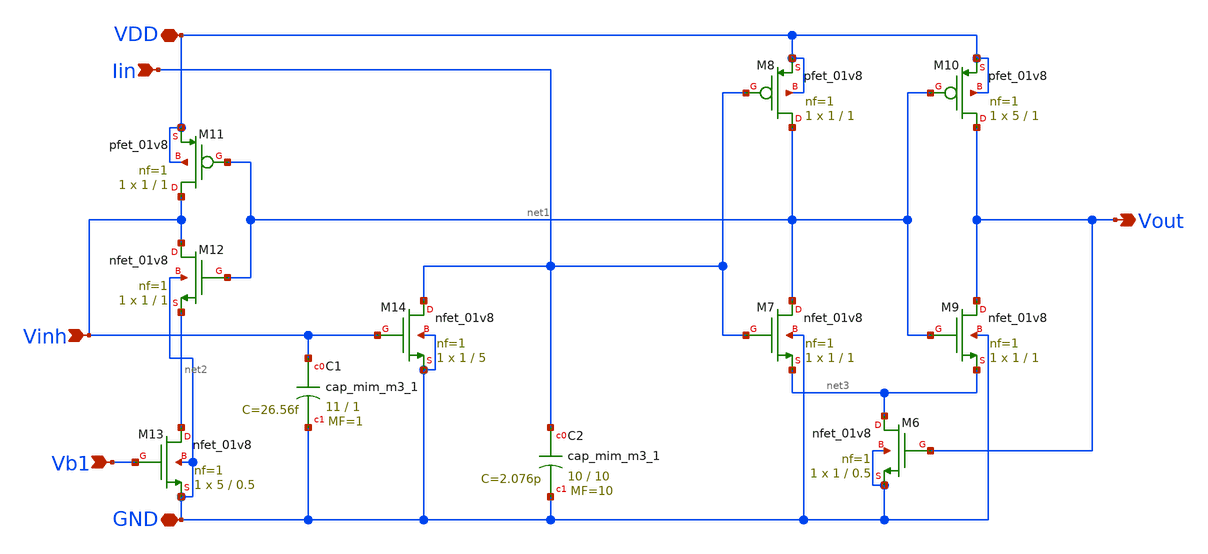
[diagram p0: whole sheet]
** sch_path: LIF_neuron/Postsynaptic_LIF_neuron.sch
**.subckt Postsynaptic_LIF_neuron GND Vb1 VDD Vout Iin Vinh
*.iopin GND
*.ipin Vb1
*.iopin VDD
*.opin Vout
*.ipin Iin
*.ipin Vinh
XM13 net2 Vb1 GND GND sky130_fd_pr__nfet_01v8 L=0.5 W=5 nf=1 ad='int((nf+1)/2) * W/nf * 0.29' as='int((nf+2)/2) * W/nf * 0.29'
+ pd='2*int((nf+1)/2) * (W/nf + 0.29)' ps='2*int((nf+2)/2) * (W/nf + 0.29)' nrd='0.29 / W' nrs='0.29 / W'
+ sa=0 sb=0 sd=0 mult=1 m=1
XM12 Vinh net1 net2 GND sky130_fd_pr__nfet_01v8 L=1 W=1 nf=1 ad='int((nf+1)/2) * W/nf * 0.29' as='int((nf+2)/2) * W/nf * 0.29'
+ pd='2*int((nf+1)/2) * (W/nf + 0.29)' ps='2*int((nf+2)/2) * (W/nf + 0.29)' nrd='0.29 / W' nrs='0.29 / W'
+ sa=0 sb=0 sd=0 mult=1 m=1
XM11 Vinh net1 VDD VDD sky130_fd_pr__pfet_01v8 L=1 W=1 nf=1 ad='int((nf+1)/2) * W/nf * 0.29' as='int((nf+2)/2) * W/nf * 0.29'
+ pd='2*int((nf+1)/2) * (W/nf + 0.29)' ps='2*int((nf+2)/2) * (W/nf + 0.29)' nrd='0.29 / W' nrs='0.29 / W'
+ sa=0 sb=0 sd=0 mult=1 m=1
XC1 Vinh GND sky130_fd_pr__cap_mim_m3_1 W=11 L=1 MF=1 m=1
XM14 Iin Vinh GND GND sky130_fd_pr__nfet_01v8 L=5 W=1 nf=1 ad='int((nf+1)/2) * W/nf * 0.29' as='int((nf+2)/2) * W/nf * 0.29'
+ pd='2*int((nf+1)/2) * (W/nf + 0.29)' ps='2*int((nf+2)/2) * (W/nf + 0.29)' nrd='0.29 / W' nrs='0.29 / W'
+ sa=0 sb=0 sd=0 mult=1 m=1
XC2 Iin GND sky130_fd_pr__cap_mim_m3_1 W=10 L=10 MF=10 m=10
XM6 net3 Vout GND GND sky130_fd_pr__nfet_01v8 L=0.5 W=1 nf=1 ad='int((nf+1)/2) * W/nf * 0.29' as='int((nf+2)/2) * W/nf * 0.29'
+ pd='2*int((nf+1)/2) * (W/nf + 0.29)' ps='2*int((nf+2)/2) * (W/nf + 0.29)' nrd='0.29 / W' nrs='0.29 / W'
+ sa=0 sb=0 sd=0 mult=1 m=1
XM7 net1 Iin net3 GND sky130_fd_pr__nfet_01v8 L=1 W=1 nf=1 ad='int((nf+1)/2) * W/nf * 0.29' as='int((nf+2)/2) * W/nf * 0.29'
+ pd='2*int((nf+1)/2) * (W/nf + 0.29)' ps='2*int((nf+2)/2) * (W/nf + 0.29)' nrd='0.29 / W' nrs='0.29 / W'
+ sa=0 sb=0 sd=0 mult=1 m=1
XM8 net1 Iin VDD VDD sky130_fd_pr__pfet_01v8 L=1 W=1 nf=1 ad='int((nf+1)/2) * W/nf * 0.29' as='int((nf+2)/2) * W/nf * 0.29'
+ pd='2*int((nf+1)/2) * (W/nf + 0.29)' ps='2*int((nf+2)/2) * (W/nf + 0.29)' nrd='0.29 / W' nrs='0.29 / W'
+ sa=0 sb=0 sd=0 mult=1 m=1
XM9 Vout net1 net3 GND sky130_fd_pr__nfet_01v8 L=1 W=1 nf=1 ad='int((nf+1)/2) * W/nf * 0.29' as='int((nf+2)/2) * W/nf * 0.29'
+ pd='2*int((nf+1)/2) * (W/nf + 0.29)' ps='2*int((nf+2)/2) * (W/nf + 0.29)' nrd='0.29 / W' nrs='0.29 / W'
+ sa=0 sb=0 sd=0 mult=1 m=1
XM10 Vout net1 VDD VDD sky130_fd_pr__pfet_01v8 L=1 W=5 nf=1 ad='int((nf+1)/2) * W/nf * 0.29' as='int((nf+2)/2) * W/nf * 0.29'
+ pd='2*int((nf+1)/2) * (W/nf + 0.29)' ps='2*int((nf+2)/2) * (W/nf + 0.29)' nrd='0.29 / W' nrs='0.29 / W'
+ sa=0 sb=0 sd=0 mult=1 m=1
**.ends
.end
